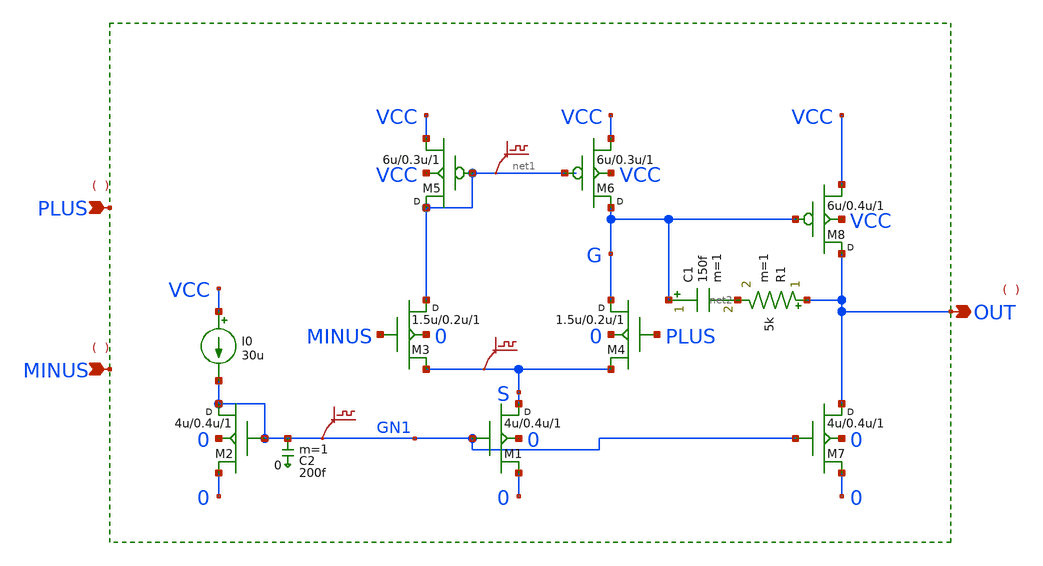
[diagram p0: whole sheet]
** sch_path: xschem_libs_newsym/ngspice/opamp_65nm/schematic/opamp_65nm.sch
* Copyright (C) 1998-2024 Stefan Frederik Schippers
* This program is free software; you can redistribute it and/or modify
* it under the terms of the GNU General Public License as published by
* the Free Software Foundation; either version 2 of the License, or
* (at your option) any later version.
* This program is distributed in the hope that it will be useful,
* but WITHOUT ANY WARRANTY; without even the implied warranty of
* MERCHANTABILITY or FITNESS FOR A PARTICULAR PURPOSE.  See the
* GNU General Public License for more details.
* You should have received a copy of the GNU General Public License
* along with this program; if not, write to the Free Software
**.subckt opamp_65nm PLUS MINUS OUT
*.ipin PLUS
*.ipin MINUS
*.opin OUT
M1 S GN1 0 0 nmos w=4u l=0.4u m=1
M2 GN1 GN1 0 0 nmos w=4u l=0.4u m=1
I0 VCC GN1 30u
M3 net1 MINUS S 0 nmos w=1.5u l=0.2u m=1
M4 G PLUS S 0 nmos w=1.5u l=0.2u m=1
M5 net1 net1 VCC VCC pmos w=6u l=0.3u m=1
M6 G net1 VCC VCC pmos w=6u l=0.3u m=1
M8 OUT G VCC VCC pmos w=6u l=0.4u m=1
.save v(gn1)
.save v(net1)
M7 OUT GN1 0 0 nmos w=4u l=0.4u m=1
R1 OUT net2 5k m=1
C1 G net2 150f m=1
C2 GN1 0 200f m=1
.save v(s)
**.ends
.end
